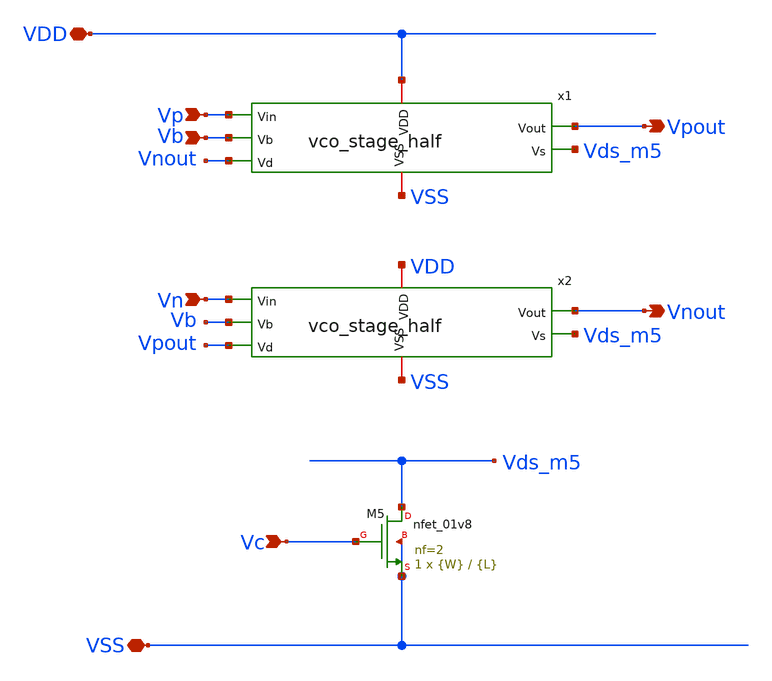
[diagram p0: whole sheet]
** sch_path: xschem/vco_stage.sch
**.subckt vco_stage VDD VSS Vp Vn Vb Vc Vpout Vnout
*.iopin VDD
*.iopin VSS
*.ipin Vp
*.ipin Vn
*.ipin Vb
*.ipin Vc
*.opin Vpout
*.opin Vnout
XM5 Vds_m5 Vc VSS VSS sky130_fd_pr__nfet_01v8 L={L} W={W} nf=2 ad='int((nf+1)/2) * W/nf * 0.29' as='int((nf+2)/2) * W/nf * 0.29'
+ pd='2*int((nf+1)/2) * (W/nf + 0.29)' ps='2*int((nf+2)/2) * (W/nf + 0.29)' nrd='0.29 / W' nrs='0.29 / W'
+ sa=0 sb=0 sd=0 mult=1 m=1
x1 VDD VSS Vp Vb Vnout Vpout Vds_m5 vco_stage_half
x2 VDD VSS Vn Vb Vpout Vnout Vds_m5 vco_stage_half
**.ends

* expanding   symbol:  vco_stage_half.sym # of pins=7
** sym_path: xschem/vco_stage_half.sym
** sch_path: xschem/vco_stage_half.sch
.subckt vco_stage_half VDD VSS Vin Vb Vd Vout Vs
*.iopin VDD
*.iopin VSS
*.ipin Vin
*.ipin Vb
*.ipin Vd
*.opin Vout
*.opin Vs
XM8 VSS Vout VSS VSS sky130_fd_pr__nfet_01v8 L={WLcap} W={WLcap} nf=1 ad='int((nf+1)/2) * W/nf * 0.29'
+ as='int((nf+2)/2) * W/nf * 0.29' pd='2*int((nf+1)/2) * (W/nf + 0.29)' ps='2*int((nf+2)/2) * (W/nf + 0.29)'
+ nrd='0.29 / W' nrs='0.29 / W' sa=0 sb=0 sd=0 mult=1 m=1
XM7 Vout Vd VDD VDD sky130_fd_pr__pfet_01v8 L={L} W={W} nf=2 ad='int((nf+1)/2) * W/nf * 0.29' as='int((nf+2)/2) * W/nf * 0.29'
+ pd='2*int((nf+1)/2) * (W/nf + 0.29)' ps='2*int((nf+2)/2) * (W/nf + 0.29)' nrd='0.29 / W' nrs='0.29 / W'
+ sa=0 sb=0 sd=0 mult=1 m=1
XM3 Vout Vb VDD VDD sky130_fd_pr__pfet_01v8 L={L} W={W} nf=2 ad='int((nf+1)/2) * W/nf * 0.29' as='int((nf+2)/2) * W/nf * 0.29'
+ pd='2*int((nf+1)/2) * (W/nf + 0.29)' ps='2*int((nf+2)/2) * (W/nf + 0.29)' nrd='0.29 / W' nrs='0.29 / W'
+ sa=0 sb=0 sd=0 mult=1 m=1
XM1 Vout Vin Vs VSS sky130_fd_pr__nfet_01v8 L={L} W={W} nf=2 ad='int((nf+1)/2) * W/nf * 0.29' as='int((nf+2)/2) * W/nf * 0.29'
+ pd='2*int((nf+1)/2) * (W/nf + 0.29)' ps='2*int((nf+2)/2) * (W/nf + 0.29)' nrd='0.29 / W' nrs='0.29 / W'
+ sa=0 sb=0 sd=0 mult=1 m=1
.ends

.end
